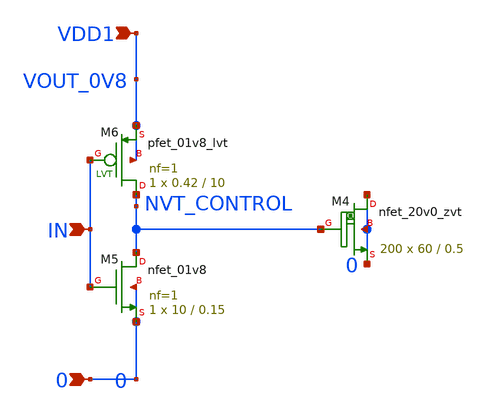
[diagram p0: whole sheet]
** sch_path: design/LELO_SVOD_SKY130A/TRANSISTOR_TEST.sch
**.subckt TRANSISTOR_TEST VDD1 0 IN
*.ipin VDD1
*.ipin 0
*.ipin IN
XM5 NVT_CONTROL IN 0 0 sky130_fd_pr__nfet_01v8 L=0.15 W=10 nf=1 ad='int((nf+1)/2) * W/nf * 0.29' as='int((nf+2)/2) * W/nf * 0.29'
+ pd='2*int((nf+1)/2) * (W/nf + 0.29)' ps='2*int((nf+2)/2) * (W/nf + 0.29)' nrd='0.29 / W' nrs='0.29 / W'
+ sa=0 sb=0 sd=0 mult=1 m=1
XM6 NVT_CONTROL IN VDD1 VDD1 sky130_fd_pr__pfet_01v8_lvt L=10 W=0.42 nf=1 ad='int((nf+1)/2) * W/nf * 0.29'
+ as='int((nf+2)/2) * W/nf * 0.29' pd='2*int((nf+1)/2) * (W/nf + 0.29)' ps='2*int((nf+2)/2) * (W/nf + 0.29)'
+ nrd='0.29 / W' nrs='0.29 / W' sa=0 sb=0 sd=0 mult=1 m=1
XM4 0 NVT_CONTROL 0 0 sky130_fd_pr__nfet_20v0_zvt W=60 L=0.5 m=200
**.ends
.end
